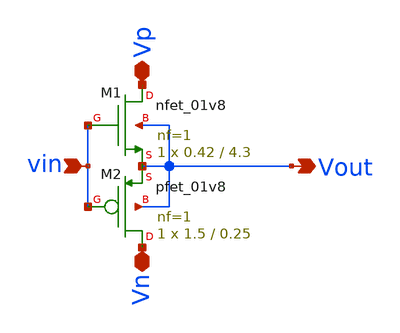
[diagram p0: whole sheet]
** sch_path: xschem/Vth_sch/op-amp.sch
**.subckt op-amp vin Vp Vn Vout
*.ipin vin
*.iopin Vp
*.iopin Vn
*.opin Vout
XM1 Vp vin Vout Vout sky130_fd_pr__nfet_01v8 L=4.3 W=0.42 nf=1 ad='int((nf+1)/2) * W/nf * 0.29' as='int((nf+2)/2) * W/nf * 0.29'
+ pd='2*int((nf+1)/2) * (W/nf + 0.29)' ps='2*int((nf+2)/2) * (W/nf + 0.29)' nrd='0.29 / W' nrs='0.29 / W'
+ sa=0 sb=0 sd=0 mult=1 m=1
XM2 Vn vin Vout Vout sky130_fd_pr__pfet_01v8 L=0.25 W=1.5 nf=1 ad='int((nf+1)/2) * W/nf * 0.29' as='int((nf+2)/2) * W/nf * 0.29'
+ pd='2*int((nf+1)/2) * (W/nf + 0.29)' ps='2*int((nf+2)/2) * (W/nf + 0.29)' nrd='0.29 / W' nrs='0.29 / W'
+ sa=0 sb=0 sd=0 mult=1 m=1
**.ends
.end
